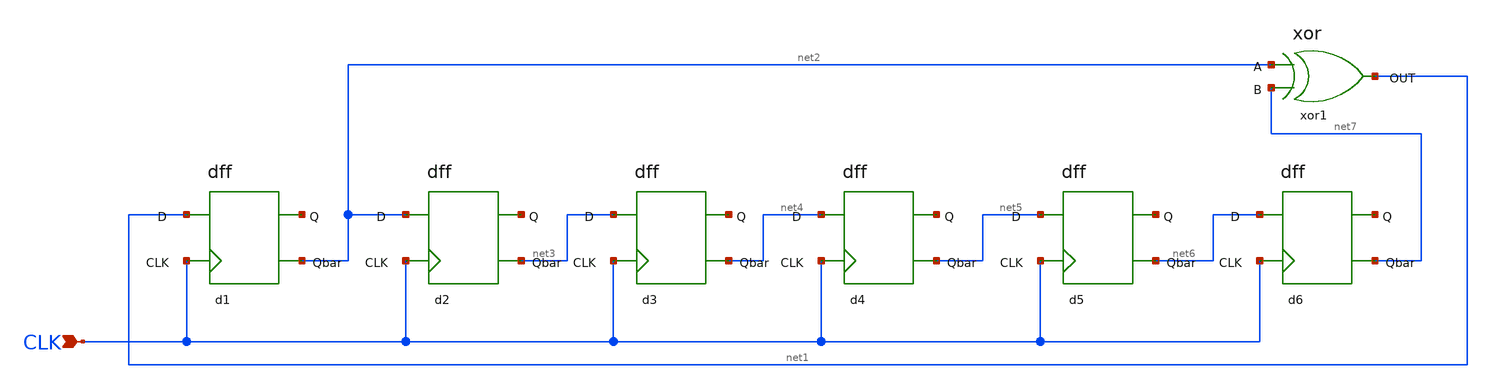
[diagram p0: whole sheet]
** sch_path: Project/1-on-chip/schematic/PNgen/pn.sch
**.subckt pn CLK
*.ipin CLK
xor1 net2 net7 net1 xor
d1 net1 CLK net8 net2 dff
d2 net2 CLK net9 net3 dff
d3 net3 CLK net10 net4 dff
d4 net4 CLK net11 net5 dff
d5 net5 CLK net12 net6 dff
d6 net6 CLK net13 net7 dff
**.ends

* expanding   symbol:  xor.sym # of pins=3
** sym_path: Project/1-on-chip/schematic/PNgen/xor.sym
** sch_path: Project/1-on-chip/schematic/PNgen/xor.sch
.subckt xor A B OUT
*.ipin A
*.opin OUT
*.ipin B
XM3 net3 A VDD VDD pfet_03v3 L=0.28u W=0.22u nf=1 ad='int((nf+1)/2) * W/nf * 0.18u' as='int((nf+2)/2) * W/nf * 0.18u'
+ pd='2*int((nf+1)/2) * (W/nf + 0.18u)' ps='2*int((nf+2)/2) * (W/nf + 0.18u)' nrd='0.18u / W' nrs='0.18u / W'
+ sa=0 sb=0 sd=0 m=1
XM4 net2 B net3 net3 pfet_03v3 L=0.28u W=0.22u nf=1 ad='int((nf+1)/2) * W/nf * 0.18u' as='int((nf+2)/2) * W/nf * 0.18u'
+ pd='2*int((nf+1)/2) * (W/nf + 0.18u)' ps='2*int((nf+2)/2) * (W/nf + 0.18u)' nrd='0.18u / W' nrs='0.18u / W'
+ sa=0 sb=0 sd=0 m=1
XM5 net4 A VDD VDD pfet_03v3 L=0.28u W=0.22u nf=1 ad='int((nf+1)/2) * W/nf * 0.18u' as='int((nf+2)/2) * W/nf * 0.18u'
+ pd='2*int((nf+1)/2) * (W/nf + 0.18u)' ps='2*int((nf+2)/2) * (W/nf + 0.18u)' nrd='0.18u / W' nrs='0.18u / W'
+ sa=0 sb=0 sd=0 m=1
XM6 net4 B VDD VDD pfet_03v3 L=0.28u W=0.22u nf=1 ad='int((nf+1)/2) * W/nf * 0.18u' as='int((nf+2)/2) * W/nf * 0.18u'
+ pd='2*int((nf+1)/2) * (W/nf + 0.18u)' ps='2*int((nf+2)/2) * (W/nf + 0.18u)' nrd='0.18u / W' nrs='0.18u / W'
+ sa=0 sb=0 sd=0 m=1
XM7 OUT net2 net4 net5 pfet_03v3 L=0.28u W=0.22u nf=1 ad='int((nf+1)/2) * W/nf * 0.18u' as='int((nf+2)/2) * W/nf * 0.18u'
+ pd='2*int((nf+1)/2) * (W/nf + 0.18u)' ps='2*int((nf+2)/2) * (W/nf + 0.18u)' nrd='0.18u / W' nrs='0.18u / W'
+ sa=0 sb=0 sd=0 m=1
XM8 OUT net2 GND GND nfet_03v3 L=0.28u W=0.22u nf=1 ad='int((nf+1)/2) * W/nf * 0.18u' as='int((nf+2)/2) * W/nf * 0.18u'
+ pd='2*int((nf+1)/2) * (W/nf + 0.18u)' ps='2*int((nf+2)/2) * (W/nf + 0.18u)' nrd='0.18u / W' nrs='0.18u / W'
+ sa=0 sb=0 sd=0 m=1
XM9 net2 A GND GND nfet_03v3 L=0.28u W=0.22u nf=1 ad='int((nf+1)/2) * W/nf * 0.18u' as='int((nf+2)/2) * W/nf * 0.18u'
+ pd='2*int((nf+1)/2) * (W/nf + 0.18u)' ps='2*int((nf+2)/2) * (W/nf + 0.18u)' nrd='0.18u / W' nrs='0.18u / W'
+ sa=0 sb=0 sd=0 m=1
XM10 net2 B GND GND nfet_03v3 L=0.28u W=0.22u nf=1 ad='int((nf+1)/2) * W/nf * 0.18u' as='int((nf+2)/2) * W/nf * 0.18u'
+ pd='2*int((nf+1)/2) * (W/nf + 0.18u)' ps='2*int((nf+2)/2) * (W/nf + 0.18u)' nrd='0.18u / W' nrs='0.18u / W'
+ sa=0 sb=0 sd=0 m=1
XM11 OUT A net1 net1 nfet_03v3 L=0.28u W=0.22u nf=1 ad='int((nf+1)/2) * W/nf * 0.18u' as='int((nf+2)/2) * W/nf * 0.18u'
+ pd='2*int((nf+1)/2) * (W/nf + 0.18u)' ps='2*int((nf+2)/2) * (W/nf + 0.18u)' nrd='0.18u / W' nrs='0.18u / W'
+ sa=0 sb=0 sd=0 m=1
XM12 net1 B GND GND nfet_03v3 L=0.28u W=0.22u nf=1 ad='int((nf+1)/2) * W/nf * 0.18u' as='int((nf+2)/2) * W/nf * 0.18u'
+ pd='2*int((nf+1)/2) * (W/nf + 0.18u)' ps='2*int((nf+2)/2) * (W/nf + 0.18u)' nrd='0.18u / W' nrs='0.18u / W'
+ sa=0 sb=0 sd=0 m=1
.ends


* expanding   symbol:  dff.sym # of pins=4
** sym_path: Project/1-on-chip/schematic/PNgen/dff.sym
** sch_path: Project/1-on-chip/schematic/PNgen/dff.sch
.subckt dff D CLK Q Qbar
*.opin Qbar
*.ipin CLK
*.ipin D
*.opin Q
XM1 net1 net3 VDD VDD pfet_03v3 L=0.28u W=0.22u nf=1 ad='int((nf+1)/2) * W/nf * 0.18u' as='int((nf+2)/2) * W/nf * 0.18u'
+ pd='2*int((nf+1)/2) * (W/nf + 0.18u)' ps='2*int((nf+2)/2) * (W/nf + 0.18u)' nrd='0.18u / W' nrs='0.18u / W'
+ sa=0 sb=0 sd=0 m=1
XM2 net1 net3 GND GND nfet_03v3 L=0.28u W=0.22u nf=1 ad='int((nf+1)/2) * W/nf * 0.18u' as='int((nf+2)/2) * W/nf * 0.18u'
+ pd='2*int((nf+1)/2) * (W/nf + 0.18u)' ps='2*int((nf+2)/2) * (W/nf + 0.18u)' nrd='0.18u / W' nrs='0.18u / W'
+ sa=0 sb=0 sd=0 m=1
XM3 net2 net1 VDD VDD pfet_03v3 L=0.28u W=0.22u nf=1 ad='int((nf+1)/2) * W/nf * 0.18u' as='int((nf+2)/2) * W/nf * 0.18u'
+ pd='2*int((nf+1)/2) * (W/nf + 0.18u)' ps='2*int((nf+2)/2) * (W/nf + 0.18u)' nrd='0.18u / W' nrs='0.18u / W'
+ sa=0 sb=0 sd=0 m=1
XM4 net2 net1 GND GND nfet_03v3 L=0.28u W=0.22u nf=1 ad='int((nf+1)/2) * W/nf * 0.18u' as='int((nf+2)/2) * W/nf * 0.18u'
+ pd='2*int((nf+1)/2) * (W/nf + 0.18u)' ps='2*int((nf+2)/2) * (W/nf + 0.18u)' nrd='0.18u / W' nrs='0.18u / W'
+ sa=0 sb=0 sd=0 m=1
XM5 Qbar net4 VDD VDD pfet_03v3 L=0.28u W=0.22u nf=1 ad='int((nf+1)/2) * W/nf * 0.18u' as='int((nf+2)/2) * W/nf * 0.18u'
+ pd='2*int((nf+1)/2) * (W/nf + 0.18u)' ps='2*int((nf+2)/2) * (W/nf + 0.18u)' nrd='0.18u / W' nrs='0.18u / W'
+ sa=0 sb=0 sd=0 m=1
XM6 Qbar net4 GND GND nfet_03v3 L=0.28u W=0.22u nf=1 ad='int((nf+1)/2) * W/nf * 0.18u' as='int((nf+2)/2) * W/nf * 0.18u'
+ pd='2*int((nf+1)/2) * (W/nf + 0.18u)' ps='2*int((nf+2)/2) * (W/nf + 0.18u)' nrd='0.18u / W' nrs='0.18u / W'
+ sa=0 sb=0 sd=0 m=1
XM7 Q Qbar VDD VDD pfet_03v3 L=0.28u W=0.22u nf=1 ad='int((nf+1)/2) * W/nf * 0.18u' as='int((nf+2)/2) * W/nf * 0.18u'
+ pd='2*int((nf+1)/2) * (W/nf + 0.18u)' ps='2*int((nf+2)/2) * (W/nf + 0.18u)' nrd='0.18u / W' nrs='0.18u / W'
+ sa=0 sb=0 sd=0 m=1
XM8 Q Qbar GND GND nfet_03v3 L=0.28u W=0.22u nf=1 ad='int((nf+1)/2) * W/nf * 0.18u' as='int((nf+2)/2) * W/nf * 0.18u'
+ pd='2*int((nf+1)/2) * (W/nf + 0.18u)' ps='2*int((nf+2)/2) * (W/nf + 0.18u)' nrd='0.18u / W' nrs='0.18u / W'
+ sa=0 sb=0 sd=0 m=1
XM9 net1 net3 GND GND nfet_03v3 L=0.28u W=0.22u nf=1 ad='int((nf+1)/2) * W/nf * 0.18u' as='int((nf+2)/2) * W/nf * 0.18u'
+ pd='2*int((nf+1)/2) * (W/nf + 0.18u)' ps='2*int((nf+2)/2) * (W/nf + 0.18u)' nrd='0.18u / W' nrs='0.18u / W'
+ sa=0 sb=0 sd=0 m=1
XM10 D CLK net3 net3 nfet_03v3 L=0.28u W=0.22u nf=1 ad='int((nf+1)/2) * W/nf * 0.18u' as='int((nf+2)/2) * W/nf * 0.18u'
+ pd='2*int((nf+1)/2) * (W/nf + 0.18u)' ps='2*int((nf+2)/2) * (W/nf + 0.18u)' nrd='0.18u / W' nrs='0.18u / W'
+ sa=0 sb=0 sd=0 m=1
XM11 net2 CLK net3 net3 pfet_03v3 L=0.28u W=0.22u nf=1 ad='int((nf+1)/2) * W/nf * 0.18u' as='int((nf+2)/2) * W/nf * 0.18u'
+ pd='2*int((nf+1)/2) * (W/nf + 0.18u)' ps='2*int((nf+2)/2) * (W/nf + 0.18u)' nrd='0.18u / W' nrs='0.18u / W'
+ sa=0 sb=0 sd=0 m=1
XM12 net4 CLK net2 net2 pfet_03v3 L=0.28u W=0.22u nf=1 ad='int((nf+1)/2) * W/nf * 0.18u' as='int((nf+2)/2) * W/nf * 0.18u'
+ pd='2*int((nf+1)/2) * (W/nf + 0.18u)' ps='2*int((nf+2)/2) * (W/nf + 0.18u)' nrd='0.18u / W' nrs='0.18u / W'
+ sa=0 sb=0 sd=0 m=1
XM13 net4 CLK Q Q nfet_03v3 L=0.28u W=0.22u nf=1 ad='int((nf+1)/2) * W/nf * 0.18u' as='int((nf+2)/2) * W/nf * 0.18u'
+ pd='2*int((nf+1)/2) * (W/nf + 0.18u)' ps='2*int((nf+2)/2) * (W/nf + 0.18u)' nrd='0.18u / W' nrs='0.18u / W'
+ sa=0 sb=0 sd=0 m=1
.ends

.GLOBAL VDD
.GLOBAL GND
.end
